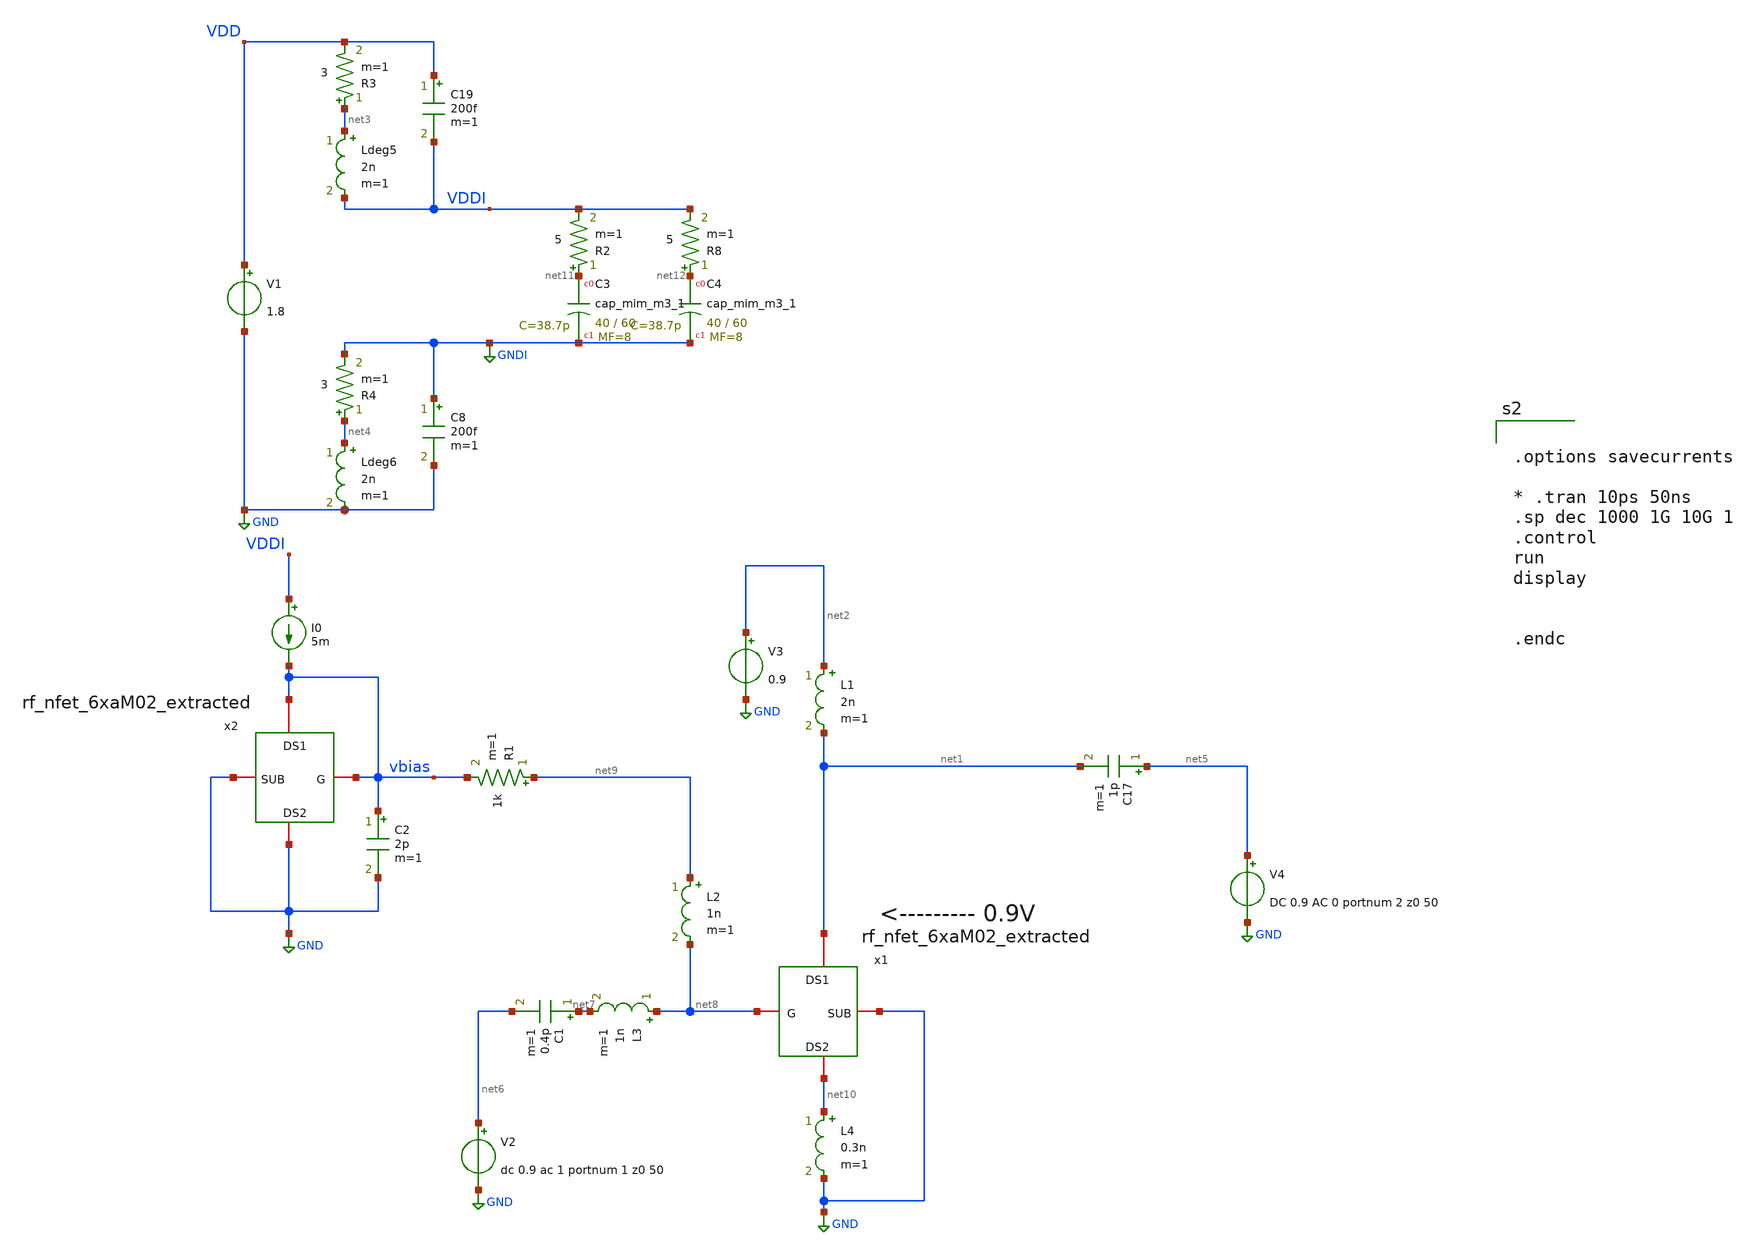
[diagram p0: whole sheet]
** sch_path: xschem/2stack_1.sch
**.subckt 2stack_1
x1 net8 net1 net10 GND rf_nfet_6xaM02_extracted
L1 net2 net1 2n m=1
V1 VDD GND 1.8
Ldeg5 net3 VDDI 2n m=1
R3 net3 VDD 3 m=1
Ldeg6 net4 GND 2n m=1
R4 net4 GNDI 3 m=1
XC3 net11 GNDI sky130_fd_pr__cap_mim_m3_1 W=40 L=60 MF=8 m=8
C8 GNDI GND 200f m=1
C19 VDD VDDI 200f m=1
R2 net11 VDDI 5 m=1
XC4 net12 GNDI sky130_fd_pr__cap_mim_m3_1 W=40 L=60 MF=8 m=8
R8 net12 VDDI 5 m=1
V2 net6 GND dc 0.9 ac 1 portnum 1 z0 50
V4 net5 GND DC 0.9 AC 0 portnum 2 z0 50
C17 net5 net1 1p m=1
L2 net9 net8 1n m=1
L3 net8 net7 1n m=1
C1 net7 net6 0.4p m=1
x2 vbias vbias GND GND rf_nfet_6xaM02_extracted
I0 VDDI vbias 5m
R1 net9 vbias 1k m=1
C2 vbias GND 2p m=1
V3 net2 GND 0.9
L4 net10 GND 0.3n m=1
**** begin user architecture code
.lib $::SKYWATER_MODELS/sky130.lib.spice tt
* .include $::PDKPATH/libs.ref/sky130_fd_sc_hvl/spice/sky130_fd_sc_hvl.spice



.options savecurrents

* .tran 10ps 50ns
.sp dec 1000 1G 10G 1
.control
run
display


.endc


**** end user architecture code
**.ends

* expanding   symbol:  rf_nfet_6xaM02_extracted.sym # of pins=4
** sym_path: xschem/rf_nfet_6xaM02_extracted.sym
** sch_path: xschem/rf_nfet_6xaM02_extracted.sch
.subckt rf_nfet_6xaM02_extracted G DS1 DS2 SUB
*.iopin G
*.iopin DS1
*.iopin DS2
*.iopin SUB
**** begin user architecture code


* Extraction of 6xaM02 (12 finger) Transistors
* wt=60um, L=0.15um
.subckt NFET_extract_1 SD1 G2 SD2 SUB

* .subckt sky130_fd_pr__rf_nfet_01v8_aM02W5p00L0p15 DRAIN GATE SOURCE SUBSTRATE
*  X0 DRAIN GATE SOURCE SUBSTRATE sky130_fd_pr__nfet_01v8 ad=1.414e+12p pd=1.066e+07u as=2.828e+12p
*+ ps=2.132e+07u w=5.05e+06u l=150000u
*  X1 SOURCE GATE DRAIN SUBSTRATE sky130_fd_pr__nfet_01v8 ad=0p pd=0u as=0p ps=0u w=5.05e+06u
*+ l=150000u
*  C0 SOURCE DRAIN 3.73fF
*  C1 SOURCE SUBSTRATE 2.58fF
* .ends

X0 SD1 G2 SD2 SUB sky130_fd_pr__nfet_01v8 ad=0p pd=0u as=0p ps=0u w=5.05e+06u l=150000u
X1 SD1 G2 SD2 SUB sky130_fd_pr__nfet_01v8 ad=0p pd=0u as=0p ps=0u w=5.05e+06u l=150000u
X2 SD2 G2 SD1 SUB sky130_fd_pr__nfet_01v8 ad=0p pd=0u as=0p ps=0u w=5.05e+06u l=150000u
X3 SD2 G2 SD1 SUB sky130_fd_pr__nfet_01v8 ad=0p pd=0u as=0p ps=0u w=5.05e+06u l=150000u
X4 SD1 G2 SD2 SUB sky130_fd_pr__nfet_01v8 ad=0p pd=0u as=0p ps=0u w=5.05e+06u l=150000u
X5 SD1 G2 SD2 SUB sky130_fd_pr__nfet_01v8 ad=0p pd=0u as=0p ps=0u w=5.05e+06u l=150000u
X6 SD2 G2 SD1 SUB sky130_fd_pr__nfet_01v8 ad=0p pd=0u as=0p ps=0u w=5.05e+06u l=150000u
X7 SD2 G2 SD1 SUB sky130_fd_pr__nfet_01v8 ad=0p pd=0u as=0p ps=0u w=5.05e+06u l=150000u
X8 SD1 G2 SD2 SUB sky130_fd_pr__nfet_01v8 ad=0p pd=0u as=0p ps=0u w=5.05e+06u l=150000u
X9 SD1 G2 SD2 SUB sky130_fd_pr__nfet_01v8 ad=0p pd=0u as=0p ps=0u w=5.05e+06u l=150000u
X10 SD2 G2 SD1 SUB sky130_fd_pr__nfet_01v8 ad=0p pd=0u as=0p ps=0u w=5.05e+06u l=150000u
X11 SD2 G2 SD1 SUB sky130_fd_pr__nfet_01v8 ad=0p pd=0u as=0p ps=0u w=5.05e+06u l=150000u
C0 SD2 G2 3.50fF
C1 SUB SD1 3.01fF
C2 G2 SD1 4.50fF
C3 G2 SUB 2.28fF
C4 SD2 SD1 30.48fF
C5 G2 SUB 3.11fF
C6 SD1 SUB 6.76fF

* C0 B G 2.85fF
* C1 S D 22.23fF
* C2 G D 5.77fF
* C3 S G 7.53fF
* Xnfet_3x_2_0/sky130_fd_pr__rf_nfet_01v8_aM02W5p00L0p15_0 D G S B
*+ sky130_fd_pr__rf_nfet_01v8_aM02W5p00L0p15
* Xnfet_3x_2_0/sky130_fd_pr__rf_nfet_01v8_aM02W5p00L0p15_1 D G S B
*+ sky130_fd_pr__rf_nfet_01v8_aM02W5p00L0p15
* Xnfet_3x_2_0/sky130_fd_pr__rf_nfet_01v8_aM02W5p00L0p15_2 D G S B
*+ sky130_fd_pr__rf_nfet_01v8_aM02W5p00L0p15
* Xnfet_3x_2_1/sky130_fd_pr__rf_nfet_01v8_aM02W5p00L0p15_0 D G S B
*+ sky130_fd_pr__rf_nfet_01v8_aM02W5p00L0p15
* Xnfet_3x_2_1/sky130_fd_pr__rf_nfet_01v8_aM02W5p00L0p15_1 D G S B
*+ sky130_fd_pr__rf_nfet_01v8_aM02W5p00L0p15
* Xnfet_3x_2_1/sky130_fd_pr__rf_nfet_01v8_aM02W5p00L0p15_2 D G S B
*+ sky130_fd_pr__rf_nfet_01v8_aM02W5p00L0p15
* C4 S B 13.70fF
* C5 G B 3.35fF

.ends

XM0 DS1 G DS2 SUB NFET_extract_1


**** end user architecture code
.ends

.GLOBAL GND
.GLOBAL GNDI
.end
